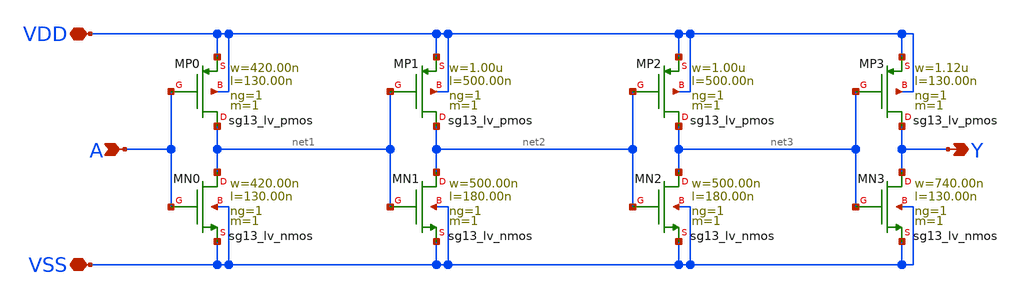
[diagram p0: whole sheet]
** sch_path: xschem/dlygate3_1.sch
**.subckt dlygate3_1 Y A VDD VSS
*.opin Y
*.ipin A
*.iopin VDD
*.iopin VSS
XMN0 net1 A VSS VSS sg13_lv_nmos w=420.00n l=130.00n ng=1 m=1 mm_ok=1
XMP0 net1 A VDD VDD sg13_lv_pmos w=420.00n l=130.00n ng=1 m=1 mm_ok=1
XMN1 net2 net1 VSS VSS sg13_lv_nmos w=500.00n l=180.00n ng=1 m=1 mm_ok=1
XMP1 net2 net1 VDD VDD sg13_lv_pmos w=1.00u l=500.00n ng=1 m=1 mm_ok=1
XMN2 net3 net2 VSS VSS sg13_lv_nmos w=500.00n l=180.00n ng=1 m=1 mm_ok=1
XMP2 net3 net2 VDD VDD sg13_lv_pmos w=1.00u l=500.00n ng=1 m=1 mm_ok=1
XMN3 Y net3 VSS VSS sg13_lv_nmos w=740.00n l=130.00n ng=1 m=1 mm_ok=1
XMP3 Y net3 VDD VDD sg13_lv_pmos w=1.12u l=130.00n ng=1 m=1 mm_ok=1
**.ends
.end
